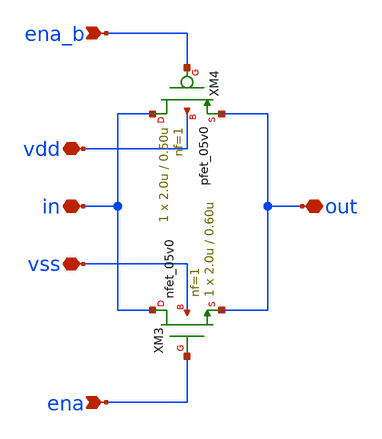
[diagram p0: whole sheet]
** sch_path: xschem/xgate.sch
**.subckt xgate out in vdd vss ena_b ena
*.iopin out
*.iopin in
*.iopin vdd
*.iopin vss
*.ipin ena_b
*.ipin ena
XM3 in ena out vss nfet_05v0 L=0.60u W=2.0u nf=1 ad='int((nf+1)/2) * W/nf * 0.18u' as='int((nf+2)/2) * W/nf * 0.18u'
+ pd='2*int((nf+1)/2) * (W/nf + 0.18u)' ps='2*int((nf+2)/2) * (W/nf + 0.18u)' nrd='0.18u / W' nrs='0.18u / W'
+ sa=0 sb=0 sd=0 m=1
XM4 in ena_b out vdd pfet_05v0 L=0.50u W=2.0u nf=1 ad='int((nf+1)/2) * W/nf * 0.18u' as='int((nf+2)/2) * W/nf * 0.18u'
+ pd='2*int((nf+1)/2) * (W/nf + 0.18u)' ps='2*int((nf+2)/2) * (W/nf + 0.18u)' nrd='0.18u / W' nrs='0.18u / W'
+ sa=0 sb=0 sd=0 m=1 par=1
**.ends
.end
